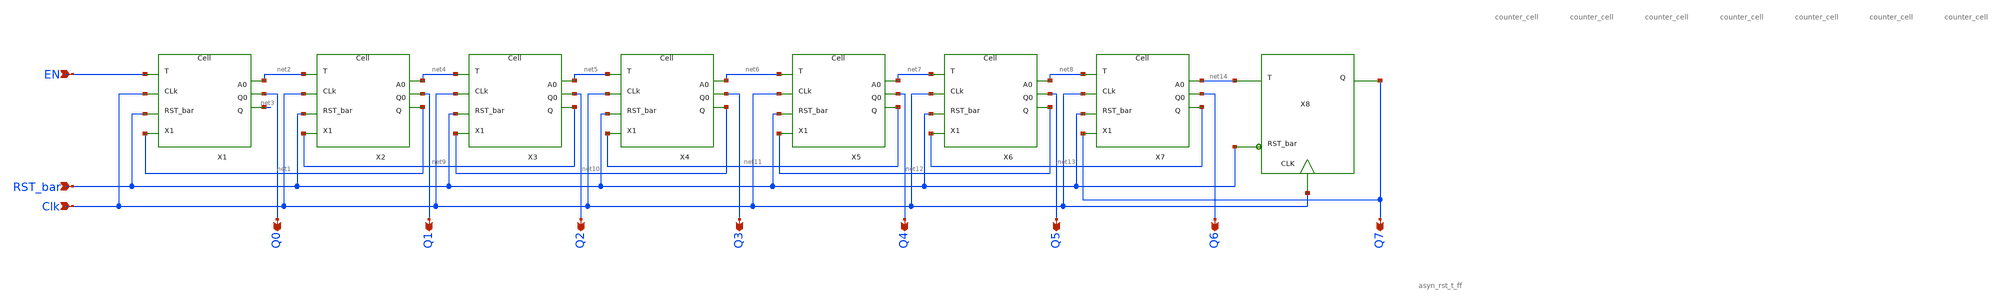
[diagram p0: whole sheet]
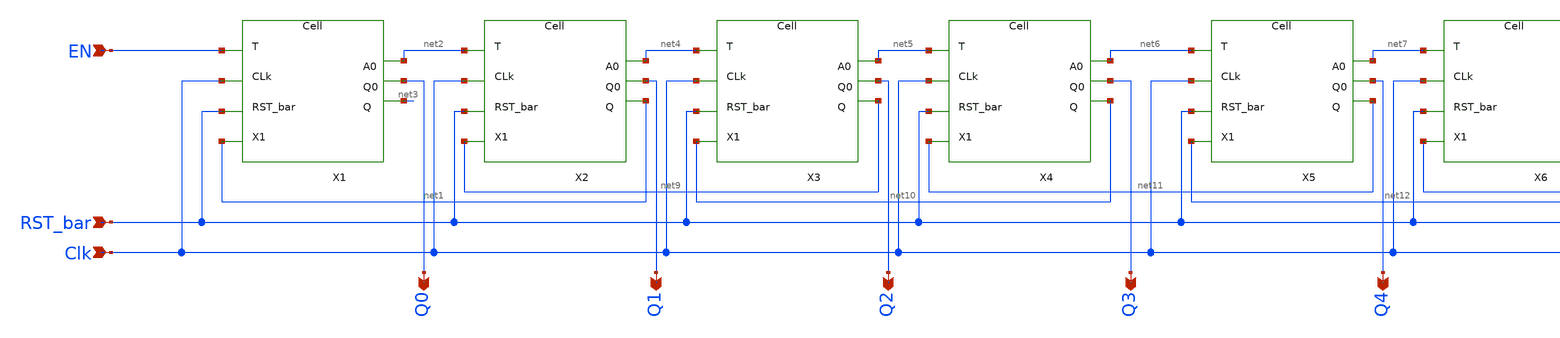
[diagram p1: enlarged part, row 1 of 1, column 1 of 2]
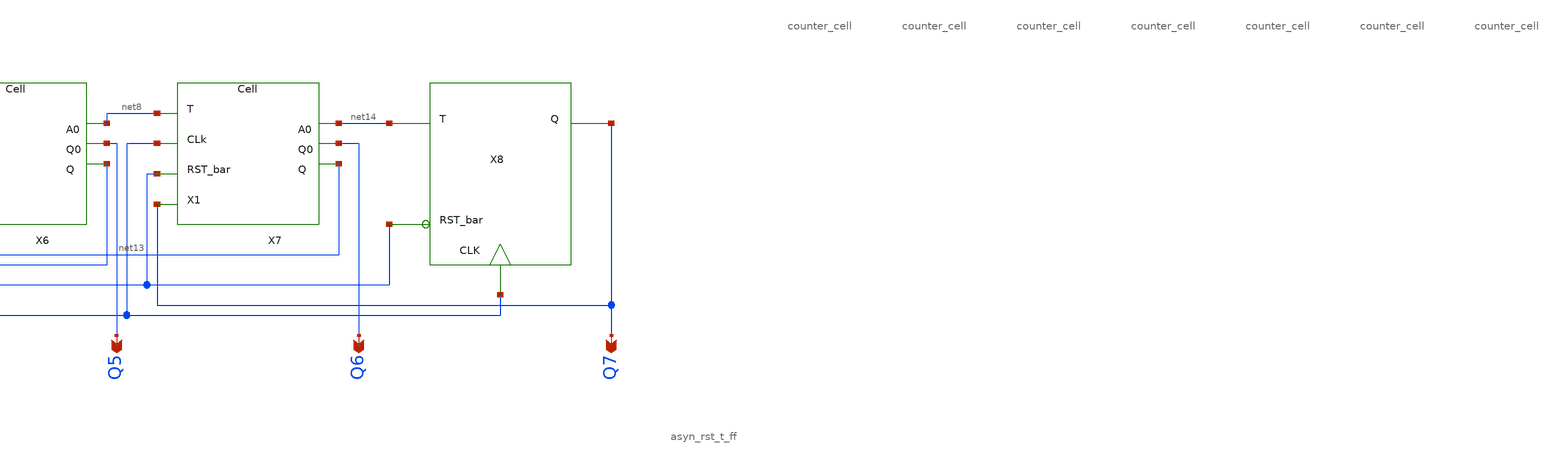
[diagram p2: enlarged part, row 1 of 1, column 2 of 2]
** sch_path: xschem/Asyn_rst_gray_counter/counter_8bit.sch
**.subckt counter_8bit EN RST_bar Clk Q0 Q1 Q2 Q3 Q4 Q5 Q6 Q7
*.ipin EN
*.ipin RST_bar
*.ipin Clk
*.opin Q0
*.opin Q1
*.opin Q2
*.opin Q3
*.opin Q4
*.opin Q5
*.opin Q6
*.opin Q7
X1 net1 RST_bar Clk EN net2 net3 Q0 counter_cell
X2 net9 RST_bar Clk net2 net4 net1 Q1 counter_cell
X3 net10 RST_bar Clk net4 net5 net9 Q2 counter_cell
X4 net11 RST_bar Clk net5 net6 net10 Q3 counter_cell
X5 net12 RST_bar Clk net6 net7 net11 Q4 counter_cell
X6 net13 RST_bar Clk net7 net8 net12 Q5 counter_cell
X7 Q7 RST_bar Clk net8 net14 net13 Q6 counter_cell
X8 net14 Q7 Clk RST_bar asyn_rst_t_ff
**.ends
.end
